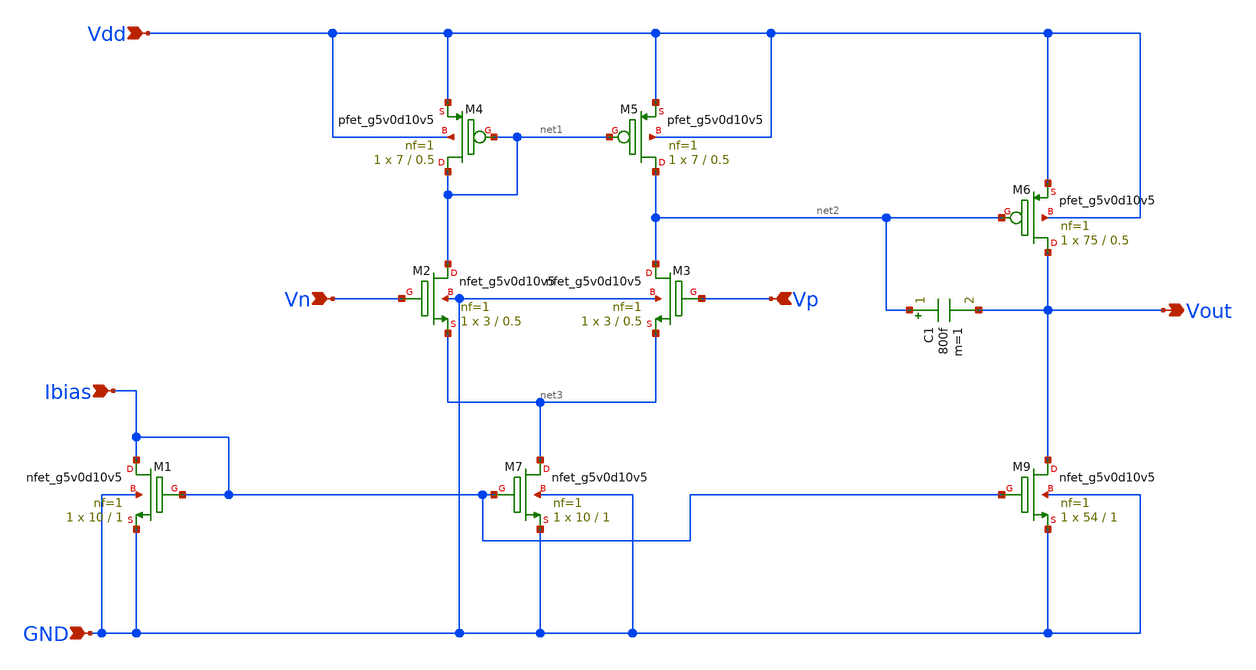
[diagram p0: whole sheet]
** sch_path: LDO/Schematic/Error_Amplifier.sch
**.subckt Error_Amplifier Vout Vdd GND Vp Vn Ibias
*.opin Vout
*.ipin Vdd
*.ipin GND
*.ipin Vp
*.ipin Vn
*.ipin Ibias
XM2 net1 Vn net3 GND sky130_fd_pr__nfet_g5v0d10v5 L=0.5 W=3 nf=1 ad='int((nf+1)/2) * W/nf * 0.29' as='int((nf+2)/2) * W/nf * 0.29'
+ pd='2*int((nf+1)/2) * (W/nf + 0.29)' ps='2*int((nf+2)/2) * (W/nf + 0.29)' nrd='0.29 / W' nrs='0.29 / W'
+ sa=0 sb=0 sd=0 mult=1 m=1
XM3 net2 Vp net3 GND sky130_fd_pr__nfet_g5v0d10v5 L=0.5 W=3 nf=1 ad='int((nf+1)/2) * W/nf * 0.29' as='int((nf+2)/2) * W/nf * 0.29'
+ pd='2*int((nf+1)/2) * (W/nf + 0.29)' ps='2*int((nf+2)/2) * (W/nf + 0.29)' nrd='0.29 / W' nrs='0.29 / W'
+ sa=0 sb=0 sd=0 mult=1 m=1
XM4 net1 net1 Vdd Vdd sky130_fd_pr__pfet_g5v0d10v5 L=0.5 W=7 nf=1 ad='int((nf+1)/2) * W/nf * 0.29' as='int((nf+2)/2) * W/nf * 0.29'
+ pd='2*int((nf+1)/2) * (W/nf + 0.29)' ps='2*int((nf+2)/2) * (W/nf + 0.29)' nrd='0.29 / W' nrs='0.29 / W'
+ sa=0 sb=0 sd=0 mult=1 m=1
XM5 net2 net1 Vdd Vdd sky130_fd_pr__pfet_g5v0d10v5 L=0.5 W=7 nf=1 ad='int((nf+1)/2) * W/nf * 0.29' as='int((nf+2)/2) * W/nf * 0.29'
+ pd='2*int((nf+1)/2) * (W/nf + 0.29)' ps='2*int((nf+2)/2) * (W/nf + 0.29)' nrd='0.29 / W' nrs='0.29 / W'
+ sa=0 sb=0 sd=0 mult=1 m=1
XM6 Vout net2 Vdd Vdd sky130_fd_pr__pfet_g5v0d10v5 L=0.5 W=75 nf=1 ad='int((nf+1)/2) * W/nf * 0.29' as='int((nf+2)/2) * W/nf * 0.29'
+ pd='2*int((nf+1)/2) * (W/nf + 0.29)' ps='2*int((nf+2)/2) * (W/nf + 0.29)' nrd='0.29 / W' nrs='0.29 / W'
+ sa=0 sb=0 sd=0 mult=1 m=1
XM7 net3 Ibias GND GND sky130_fd_pr__nfet_g5v0d10v5 L=1 W=10 nf=1 ad='int((nf+1)/2) * W/nf * 0.29' as='int((nf+2)/2) * W/nf * 0.29'
+ pd='2*int((nf+1)/2) * (W/nf + 0.29)' ps='2*int((nf+2)/2) * (W/nf + 0.29)' nrd='0.29 / W' nrs='0.29 / W'
+ sa=0 sb=0 sd=0 mult=1 m=1
XM9 Vout Ibias GND GND sky130_fd_pr__nfet_g5v0d10v5 L=1 W=54 nf=1 ad='int((nf+1)/2) * W/nf * 0.29' as='int((nf+2)/2) * W/nf * 0.29'
+ pd='2*int((nf+1)/2) * (W/nf + 0.29)' ps='2*int((nf+2)/2) * (W/nf + 0.29)' nrd='0.29 / W' nrs='0.29 / W'
+ sa=0 sb=0 sd=0 mult=1 m=1
XM1 Ibias Ibias GND GND sky130_fd_pr__nfet_g5v0d10v5 L=1 W=10 nf=1 ad='int((nf+1)/2) * W/nf * 0.29' as='int((nf+2)/2) * W/nf * 0.29'
+ pd='2*int((nf+1)/2) * (W/nf + 0.29)' ps='2*int((nf+2)/2) * (W/nf + 0.29)' nrd='0.29 / W' nrs='0.29 / W'
+ sa=0 sb=0 sd=0 mult=1 m=1
C1 net2 Vout 800f m=1
**.ends
.end
